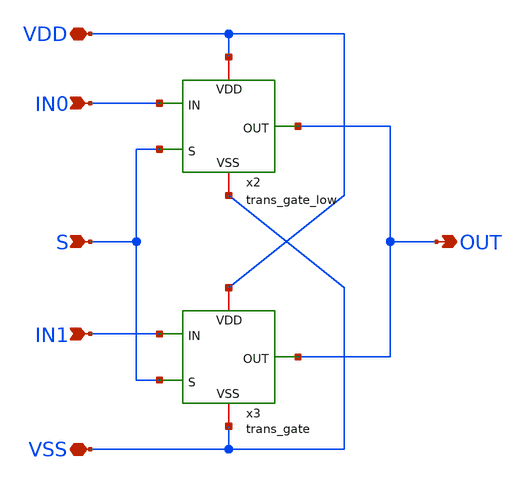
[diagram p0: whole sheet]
** sch_path: SSDOR_1V_v1/components/mux2/mux2.sch
**.subckt mux2 IN0 S IN1 VDD VSS OUT
*.ipin IN0
*.ipin S
*.ipin IN1
*.iopin VDD
*.iopin VSS
*.opin OUT
x3 OUT IN1 VDD S VSS trans_gate
x2 OUT IN0 VDD S VSS trans_gate_low
**.ends
.end
